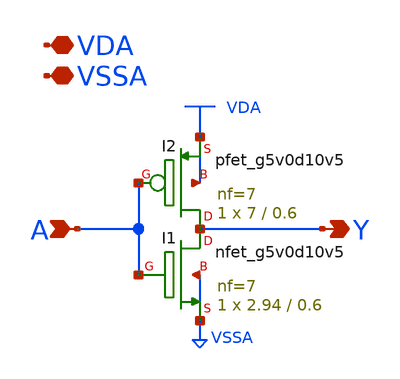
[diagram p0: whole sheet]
** sch_path: gpiov2_amx_pucsd_inv.sch
* Copyright 2023 David Mitchell Bailey
* Licensed under the Apache License, Version 2.0 (the "License");
* you may not use this file except in compliance with the License.
* You may obtain a copy of the License at
* https://www.apache.org/licenses/LICENSE-2.0
* Unless required by applicable law or agreed to in writing, software
* distributed under the License is distributed on an "AS IS" BASIS,
* WITHOUT WARRANTIES OR CONDITIONS OF ANY KIND, either express or implied.
* See the License for the specific language governing permissions and
* limitations under the License.
**.subckt gpiov2_amx_pucsd_inv A Y VDA VSSA
*.ipin A
*.opin Y
*.iopin VDA
*.iopin VSSA
XI1 Y A VSSA VSSA sky130_fd_pr__nfet_g5v0d10v5 L=0.6 W=2.94 nf=7 ad='int((nf+1)/2) * W/nf * 0.29' as='int((nf+2)/2) * W/nf * 0.29'
+ pd='2*int((nf+1)/2) * (W/nf + 0.29)' ps='2*int((nf+2)/2) * (W/nf + 0.29)' nrd='0.29 / W' nrs='0.29 / W'
+ sa=0 sb=0 sd=0 mult=1 m=1
XI2 Y A VDA VDA sky130_fd_pr__pfet_g5v0d10v5 L=0.6 W=7 nf=7 ad='int((nf+1)/2) * W/nf * 0.29' as='int((nf+2)/2) * W/nf * 0.29'
+ pd='2*int((nf+1)/2) * (W/nf + 0.29)' ps='2*int((nf+2)/2) * (W/nf + 0.29)' nrd='0.29 / W' nrs='0.29 / W'
+ sa=0 sb=0 sd=0 mult=1 m=1
**.ends
.end
